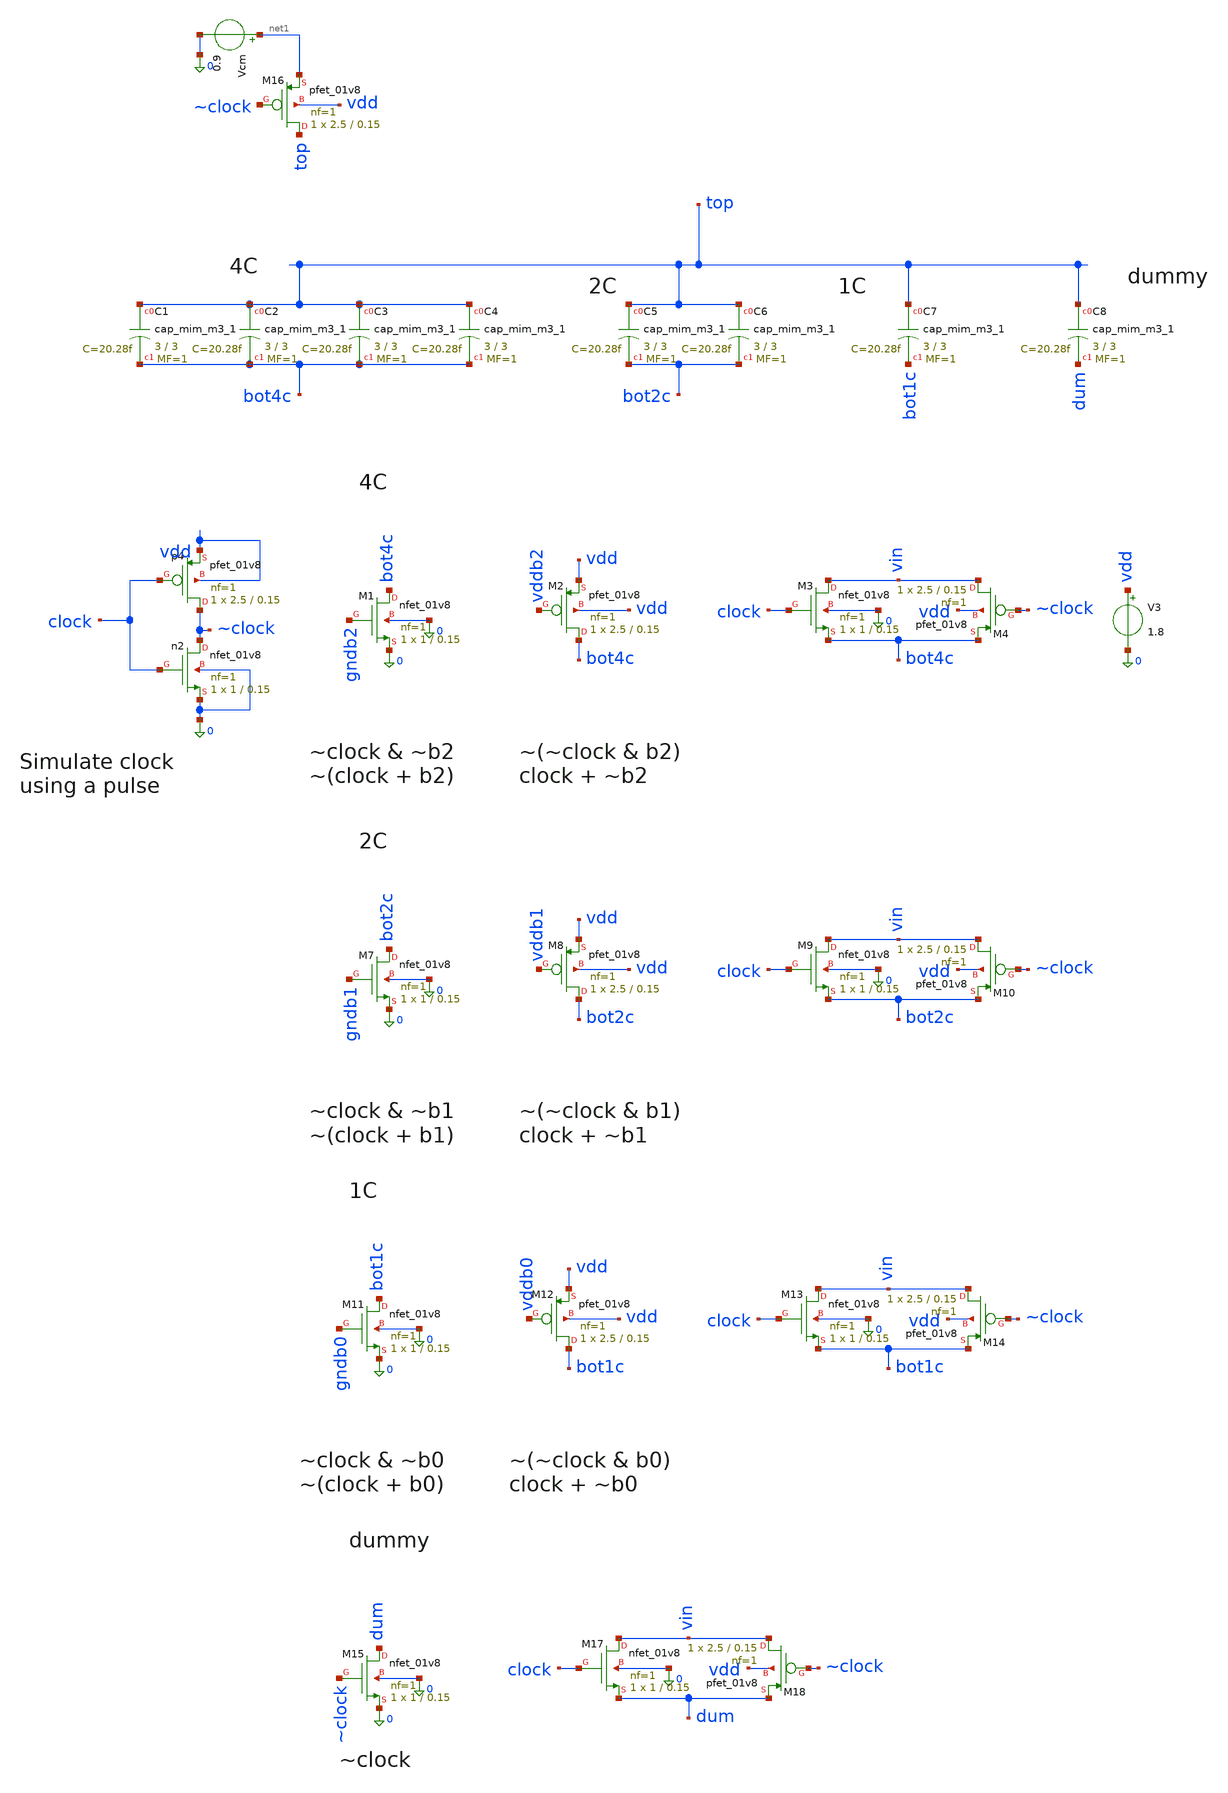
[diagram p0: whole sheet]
** sch_path: analog/cdac/cdac.sch
**.subckt cdac
XC1 top bot4c sky130_fd_pr__cap_mim_m3_1 W=3 L=3 MF=1 m=1
XC2 top bot4c sky130_fd_pr__cap_mim_m3_1 W=3 L=3 MF=1 m=1
XC3 top bot4c sky130_fd_pr__cap_mim_m3_1 W=3 L=3 MF=1 m=1
XC4 top bot4c sky130_fd_pr__cap_mim_m3_1 W=3 L=3 MF=1 m=1
XC5 top bot2c sky130_fd_pr__cap_mim_m3_1 W=3 L=3 MF=1 m=1
XC6 top bot2c sky130_fd_pr__cap_mim_m3_1 W=3 L=3 MF=1 m=1
XC7 top bot1c sky130_fd_pr__cap_mim_m3_1 W=3 L=3 MF=1 m=1
XC8 top dum sky130_fd_pr__cap_mim_m3_1 W=3 L=3 MF=1 m=1
Xn2 ~clock clock 0 0 sky130_fd_pr__nfet_01v8 L=0.15 W=1 nf=1 ad='int((1 + 1)/2) * 1 / 1 * 0.29' as='int((1 + 2)/2) * 1 / 1 * 0.29'
+ pd='2*int((1 + 1)/2) * (1 / 1 + 0.29)' ps='2*int((1 + 2)/2) * (1 / 1 + 0.29)' nrd='0.29 / 1 ' nrs='0.29 / 1 '
+ sa=0 sb=0 sd=0 mult=1 m=1
Xp4 ~clock clock vdd vdd sky130_fd_pr__pfet_01v8 L=0.15 W=2.5 nf=1 ad='int((1 + 1)/2) * 2.5 / 1 * 0.29'
+ as='int((1 + 2)/2) * 2.5 / 1 * 0.29' pd='2*int((1 + 1)/2) * (2.5 / 1 + 0.29)' ps='2*int((1 + 2)/2) * (2.5 / 1 + 0.29)'
+ nrd='0.29 / 2.5 ' nrs='0.29 / 2.5 ' sa=0 sb=0 sd=0 mult=1 m=1
XM1 bot4c gndb2 0 0 sky130_fd_pr__nfet_01v8 L=0.15 W=1 nf=1 ad='int((1 + 1)/2) * 1 / 1 * 0.29' as='int((1 + 2)/2) * 1 / 1 * 0.29'
+ pd='2*int((1 + 1)/2) * (1 / 1 + 0.29)' ps='2*int((1 + 2)/2) * (1 / 1 + 0.29)' nrd='0.29 / 1 ' nrs='0.29 / 1 '
+ sa=0 sb=0 sd=0 mult=1 m=1
XM2 bot4c vddb2 vdd vdd sky130_fd_pr__pfet_01v8 L=0.15 W=2.5 nf=1 ad='int((1 + 1)/2) * 2.5 / 1 * 0.29'
+ as='int((1 + 2)/2) * 2.5 / 1 * 0.29' pd='2*int((1 + 1)/2) * (2.5 / 1 + 0.29)' ps='2*int((1 + 2)/2) * (2.5 / 1 + 0.29)'
+ nrd='0.29 / 2.5 ' nrs='0.29 / 2.5 ' sa=0 sb=0 sd=0 mult=1 m=1
XM3 vin clock bot4c 0 sky130_fd_pr__nfet_01v8 L=0.15 W=1 nf=1 ad='int((1 + 1)/2) * 1 / 1 * 0.29' as='int((1 + 2)/2) * 1 / 1 * 0.29'
+ pd='2*int((1 + 1)/2) * (1 / 1 + 0.29)' ps='2*int((1 + 2)/2) * (1 / 1 + 0.29)' nrd='0.29 / 1 ' nrs='0.29 / 1 '
+ sa=0 sb=0 sd=0 mult=1 m=1
XM4 vin ~clock bot4c vdd sky130_fd_pr__pfet_01v8 L=0.15 W=2.5 nf=1 ad='int((1 + 1)/2) * 2.5 / 1 * 0.29'
+ as='int((1 + 2)/2) * 2.5 / 1 * 0.29' pd='2*int((1 + 1)/2) * (2.5 / 1 + 0.29)' ps='2*int((1 + 2)/2) * (2.5 / 1 + 0.29)'
+ nrd='0.29 / 2.5 ' nrs='0.29 / 2.5 ' sa=0 sb=0 sd=0 mult=1 m=1
V3 vdd 0 1.8
XM7 bot2c gndb1 0 0 sky130_fd_pr__nfet_01v8 L=0.15 W=1 nf=1 ad='int((1 + 1)/2) * 1 / 1 * 0.29' as='int((1 + 2)/2) * 1 / 1 * 0.29'
+ pd='2*int((1 + 1)/2) * (1 / 1 + 0.29)' ps='2*int((1 + 2)/2) * (1 / 1 + 0.29)' nrd='0.29 / 1 ' nrs='0.29 / 1 '
+ sa=0 sb=0 sd=0 mult=1 m=1
XM8 bot2c vddb1 vdd vdd sky130_fd_pr__pfet_01v8 L=0.15 W=2.5 nf=1 ad='int((1 + 1)/2) * 2.5 / 1 * 0.29'
+ as='int((1 + 2)/2) * 2.5 / 1 * 0.29' pd='2*int((1 + 1)/2) * (2.5 / 1 + 0.29)' ps='2*int((1 + 2)/2) * (2.5 / 1 + 0.29)'
+ nrd='0.29 / 2.5 ' nrs='0.29 / 2.5 ' sa=0 sb=0 sd=0 mult=1 m=1
XM9 vin clock bot2c 0 sky130_fd_pr__nfet_01v8 L=0.15 W=1 nf=1 ad='int((1 + 1)/2) * 1 / 1 * 0.29' as='int((1 + 2)/2) * 1 / 1 * 0.29'
+ pd='2*int((1 + 1)/2) * (1 / 1 + 0.29)' ps='2*int((1 + 2)/2) * (1 / 1 + 0.29)' nrd='0.29 / 1 ' nrs='0.29 / 1 '
+ sa=0 sb=0 sd=0 mult=1 m=1
XM10 vin ~clock bot2c vdd sky130_fd_pr__pfet_01v8 L=0.15 W=2.5 nf=1 ad='int((1 + 1)/2) * 2.5 / 1 * 0.29'
+ as='int((1 + 2)/2) * 2.5 / 1 * 0.29' pd='2*int((1 + 1)/2) * (2.5 / 1 + 0.29)' ps='2*int((1 + 2)/2) * (2.5 / 1 + 0.29)'
+ nrd='0.29 / 2.5 ' nrs='0.29 / 2.5 ' sa=0 sb=0 sd=0 mult=1 m=1
XM11 bot1c gndb0 0 0 sky130_fd_pr__nfet_01v8 L=0.15 W=1 nf=1 ad='int((1 + 1)/2) * 1 / 1 * 0.29' as='int((1 + 2)/2) * 1 / 1 * 0.29'
+ pd='2*int((1 + 1)/2) * (1 / 1 + 0.29)' ps='2*int((1 + 2)/2) * (1 / 1 + 0.29)' nrd='0.29 / 1 ' nrs='0.29 / 1 '
+ sa=0 sb=0 sd=0 mult=1 m=1
XM12 bot1c vddb0 vdd vdd sky130_fd_pr__pfet_01v8 L=0.15 W=2.5 nf=1 ad='int((1 + 1)/2) * 2.5 / 1 * 0.29'
+ as='int((1 + 2)/2) * 2.5 / 1 * 0.29' pd='2*int((1 + 1)/2) * (2.5 / 1 + 0.29)' ps='2*int((1 + 2)/2) * (2.5 / 1 + 0.29)'
+ nrd='0.29 / 2.5 ' nrs='0.29 / 2.5 ' sa=0 sb=0 sd=0 mult=1 m=1
XM13 vin clock bot1c 0 sky130_fd_pr__nfet_01v8 L=0.15 W=1 nf=1 ad='int((1 + 1)/2) * 1 / 1 * 0.29' as='int((1 + 2)/2) * 1 / 1 * 0.29'
+ pd='2*int((1 + 1)/2) * (1 / 1 + 0.29)' ps='2*int((1 + 2)/2) * (1 / 1 + 0.29)' nrd='0.29 / 1 ' nrs='0.29 / 1 '
+ sa=0 sb=0 sd=0 mult=1 m=1
XM14 vin ~clock bot1c vdd sky130_fd_pr__pfet_01v8 L=0.15 W=2.5 nf=1 ad='int((1 + 1)/2) * 2.5 / 1 * 0.29'
+ as='int((1 + 2)/2) * 2.5 / 1 * 0.29' pd='2*int((1 + 1)/2) * (2.5 / 1 + 0.29)' ps='2*int((1 + 2)/2) * (2.5 / 1 + 0.29)'
+ nrd='0.29 / 2.5 ' nrs='0.29 / 2.5 ' sa=0 sb=0 sd=0 mult=1 m=1
XM15 dum ~clock 0 0 sky130_fd_pr__nfet_01v8 L=0.15 W=1 nf=1 ad='int((1 + 1)/2) * 1 / 1 * 0.29' as='int((1 + 2)/2) * 1 / 1 * 0.29'
+ pd='2*int((1 + 1)/2) * (1 / 1 + 0.29)' ps='2*int((1 + 2)/2) * (1 / 1 + 0.29)' nrd='0.29 / 1 ' nrs='0.29 / 1 '
+ sa=0 sb=0 sd=0 mult=1 m=1
XM17 vin clock dum 0 sky130_fd_pr__nfet_01v8 L=0.15 W=1 nf=1 ad='int((1 + 1)/2) * 1 / 1 * 0.29' as='int((1 + 2)/2) * 1 / 1 * 0.29'
+ pd='2*int((1 + 1)/2) * (1 / 1 + 0.29)' ps='2*int((1 + 2)/2) * (1 / 1 + 0.29)' nrd='0.29 / 1 ' nrs='0.29 / 1 '
+ sa=0 sb=0 sd=0 mult=1 m=1
XM18 vin ~clock dum vdd sky130_fd_pr__pfet_01v8 L=0.15 W=2.5 nf=1 ad='int((1 + 1)/2) * 2.5 / 1 * 0.29'
+ as='int((1 + 2)/2) * 2.5 / 1 * 0.29' pd='2*int((1 + 1)/2) * (2.5 / 1 + 0.29)' ps='2*int((1 + 2)/2) * (2.5 / 1 + 0.29)'
+ nrd='0.29 / 2.5 ' nrs='0.29 / 2.5 ' sa=0 sb=0 sd=0 mult=1 m=1
Vcm net1 0 0.9
XM16 top ~clock net1 vdd sky130_fd_pr__pfet_01v8 L=0.15 W=2.5 nf=1 ad='int((1 + 1)/2) * 2.5 / 1 * 0.29'
+ as='int((1 + 2)/2) * 2.5 / 1 * 0.29' pd='2*int((1 + 1)/2) * (2.5 / 1 + 0.29)' ps='2*int((1 + 2)/2) * (2.5 / 1 + 0.29)'
+ nrd='0.29 / 2.5 ' nrs='0.29 / 2.5 ' sa=0 sb=0 sd=0 mult=1 m=1
**.ends
.end
